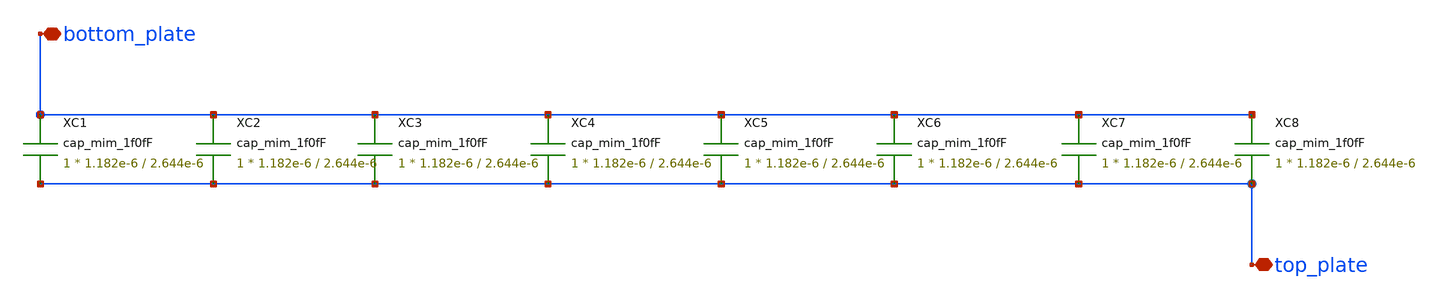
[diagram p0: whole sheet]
** sch_path: CDAC/8C.sch
**.subckt 8C bottom_plate top_plate
*.iopin bottom_plate
*.iopin top_plate
XC2 bottom_plate top_plate cap_mim_1f0fF c_width=1.182e-6 c_length=2.644e-6 m=1
XC3 bottom_plate top_plate cap_mim_1f0fF c_width=1.182e-6 c_length=2.644e-6 m=1
XC4 bottom_plate top_plate cap_mim_1f0fF c_width=1.182e-6 c_length=2.644e-6 m=1
XC5 bottom_plate top_plate cap_mim_1f0fF c_width=1.182e-6 c_length=2.644e-6 m=1
XC6 bottom_plate top_plate cap_mim_1f0fF c_width=1.182e-6 c_length=2.644e-6 m=1
XC7 bottom_plate top_plate cap_mim_1f0fF c_width=1.182e-6 c_length=2.644e-6 m=1
XC8 bottom_plate top_plate cap_mim_1f0fF c_width=1.182e-6 c_length=2.644e-6 m=1
XC1 bottom_plate top_plate cap_mim_1f0fF c_width=1.182e-6 c_length=2.644e-6 m=1
**.ends
.end
